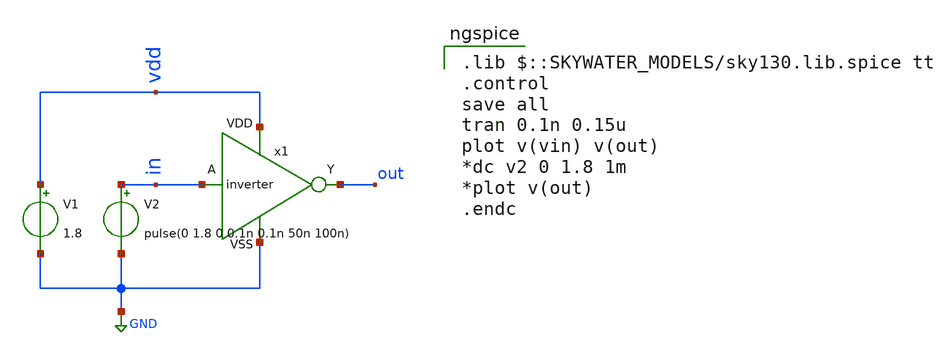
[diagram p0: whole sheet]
** sch_path: images/align/design/Examples/Inverter/inverter_tb.sch
**.subckt inverter_tb
V1 vdd GND 1.8
V2 in GND pulse(0 1.8 0 0.1n 0.1n 50n 100n)
x1 vdd in out GND inverter
**** begin user architecture code
 .lib $::SKYWATER_MODELS/sky130.lib.spice tt
.control
save all
tran 0.1n 0.15u
plot v(vin) v(out)
*dc v2 0 1.8 1m
*plot v(out)
.endc
**** end user architecture code
**.ends

* expanding   symbol:  inverter.sym # of pins=4
** sym_path: images/align/design/Example/Inverter/inverter.sym
** sch_path: images/align/design/Example/Inverter/inverter.sch
.subckt inverter VDD A Y VSS
*.ipin A
*.opin Y
*.iopin VDD
*.iopin VSS
.param Wn=1.05
.param L=0.15
.param Wp=0.84
XM2 Y A VDD VDD sky130_fd_pr__pfet_01v8 L=L W='Wp * 2' nf=2 ad='int((nf+1)/2) * W/nf * 0.29' as='int((nf+2)/2) * W/nf * 0.29'
+ pd='2*int((nf+1)/2) * (W/nf + 0.29)' ps='2*int((nf+2)/2) * (W/nf + 0.29)' nrd='0.29 / W' nrs='0.29 / W'
+ sa=0 sb=0 sd=0 mult=1 m=1
XM1 Y A VSS VSS sky130_fd_pr__nfet_01v8 L=L W='Wn * 2' nf=2 ad='int((nf+1)/2) * W/nf * 0.29' as='int((nf+2)/2) * W/nf * 0.29'
+ pd='2*int((nf+1)/2) * (W/nf + 0.29)' ps='2*int((nf+2)/2) * (W/nf + 0.29)' nrd='0.29 / W' nrs='0.29 / W'
+ sa=0 sb=0 sd=0 mult=1 m=1
.ends

.GLOBAL GND
.end
